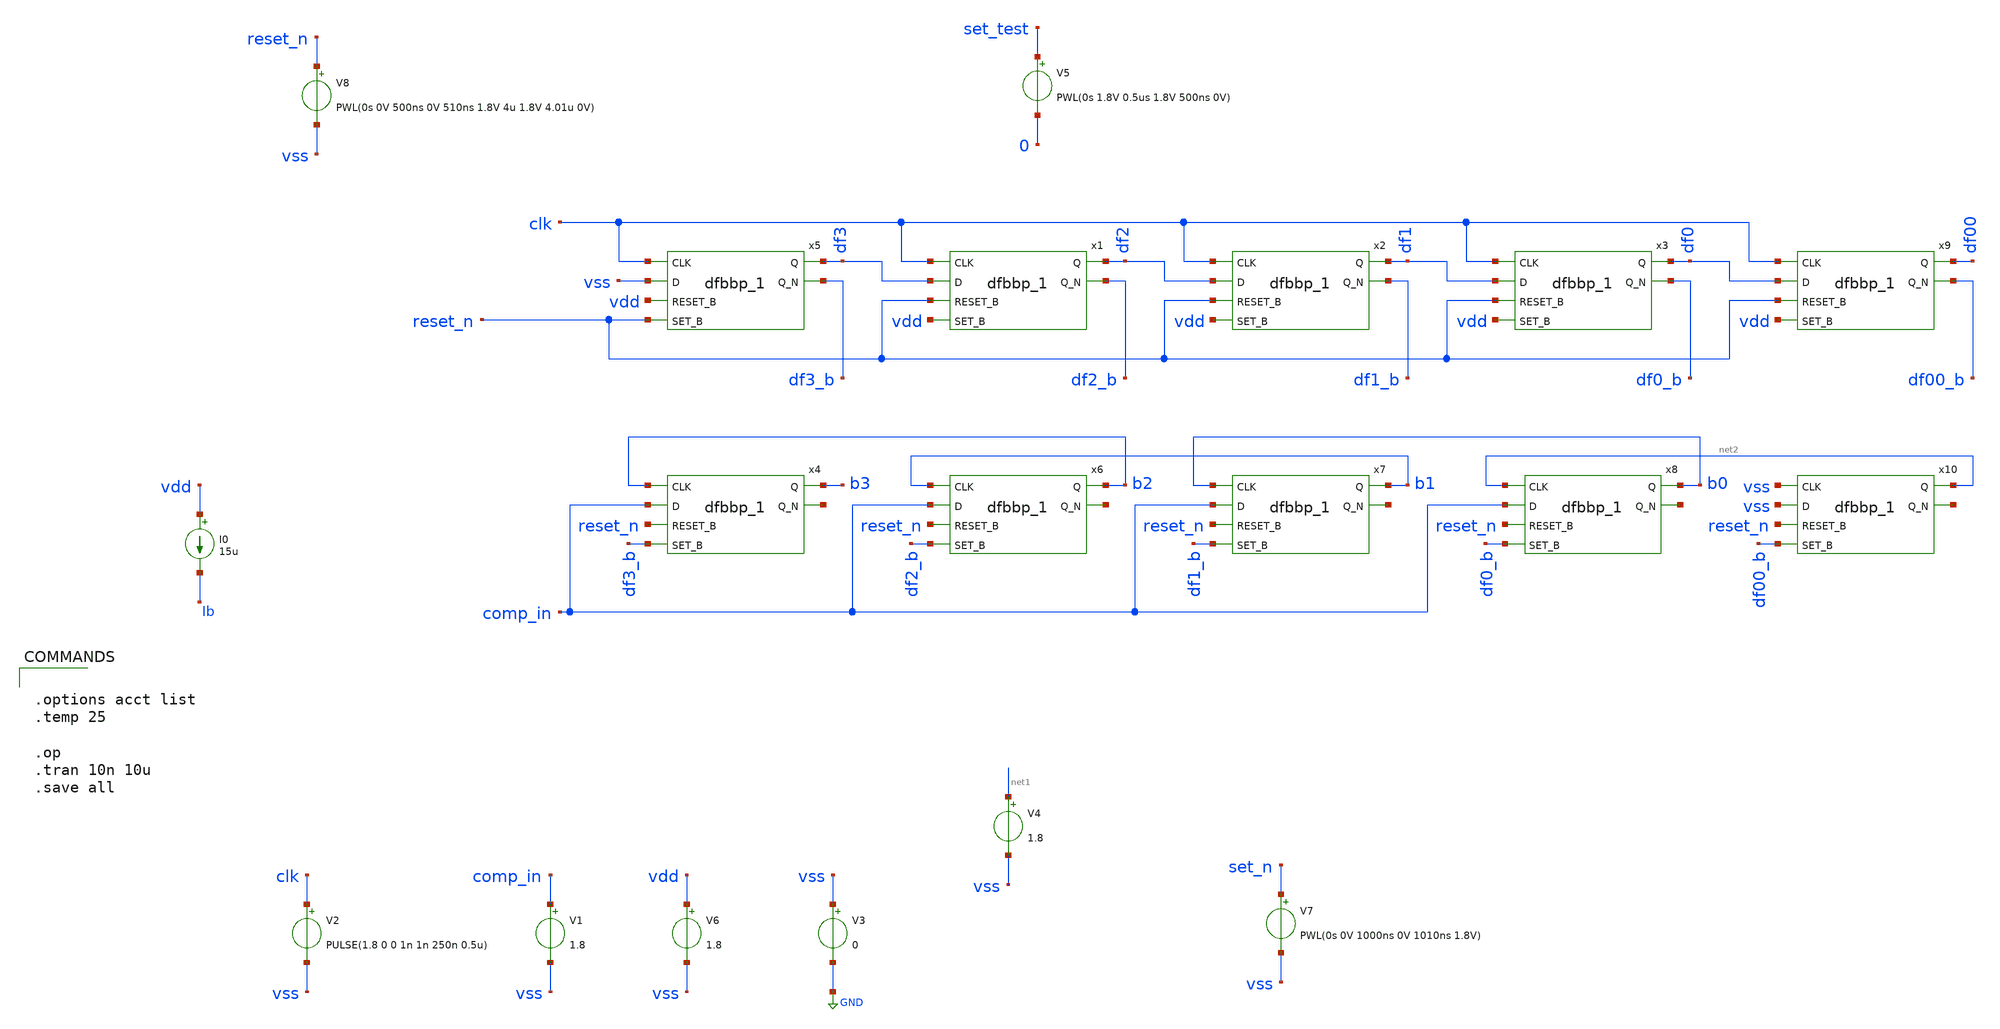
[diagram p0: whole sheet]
** sch_path: xschem/sar_logic/sar_logic_tb.sch
.lib $::SKYWATER_MODELS/sky130.lib.spice tt
.include $::SKYWATER_STDCELLS/sky130_fd_sc_hd.spice

**.subckt sar_logic_tb
V2 clk vss PULSE(1.8 0 0 1n 1n 250n 0.5u)
V1 comp_in vss 1.8
V4 net1 vss 1.8
V5 set_test 0 PWL(0s 1.8V 0.5us 1.8V 500ns 0V)
V6 vdd vss 1.8
V7 set_n vss PWL(0s 0V 1000ns 0V 1010ns 1.8V)
V3 vss GND 0
I0 vdd Ib 15u
x5 clk vss vdd reset_n vss vss vdd vdd df3 df3_b sky130_fd_sc_hd__dfbbp_1
x1 clk df3 reset_n vdd vss vss vdd vdd df2 df2_b sky130_fd_sc_hd__dfbbp_1
x2 clk df2 reset_n vdd vss vss vdd vdd df1 df1_b sky130_fd_sc_hd__dfbbp_1
x3 clk df1 reset_n vdd vss vss vdd vdd df0 df0_b sky130_fd_sc_hd__dfbbp_1
x4 b2 comp_in reset_n df3_b vss vss vdd vdd b3 net3 sky130_fd_sc_hd__dfbbp_1
x6 b1 comp_in reset_n df2_b vss vss vdd vdd b2 net4 sky130_fd_sc_hd__dfbbp_1
x7 b0 comp_in reset_n df1_b vss vss vdd vdd b1 net5 sky130_fd_sc_hd__dfbbp_1
x8 net2 comp_in reset_n df0_b vss vss vdd vdd b0 net6 sky130_fd_sc_hd__dfbbp_1
x9 clk df0 reset_n vdd vss vss vdd vdd df00 df00_b sky130_fd_sc_hd__dfbbp_1
x10 vss vss reset_n df00_b vss vss vdd vdd net2 net7 sky130_fd_sc_hd__dfbbp_1
V8 reset_n vss PWL(0s 0V 500ns 0V 510ns 1.8V 4u 1.8V 4.01u 0V)
**** begin user architecture code


.options acct list
.temp 25

.op
.tran 10n 10u
.save all


**** end user architecture code
**.ends
.GLOBAL GND
.end
